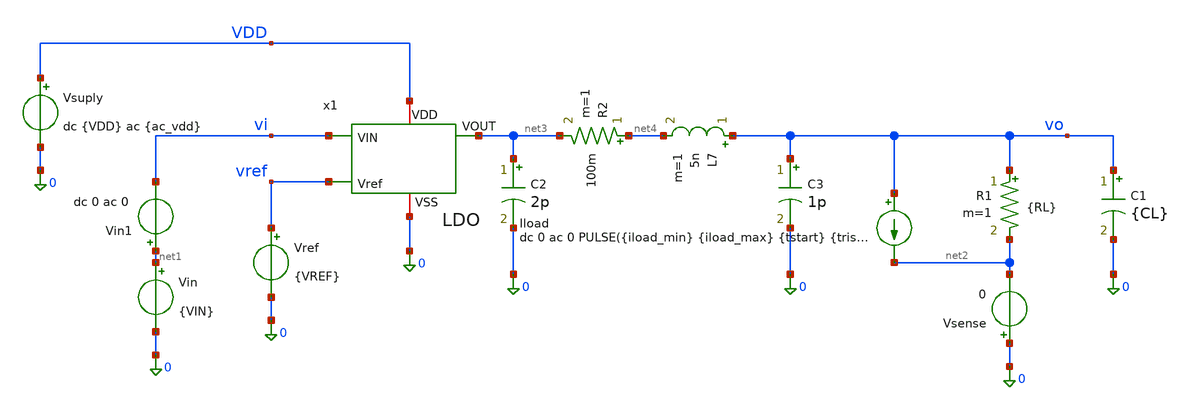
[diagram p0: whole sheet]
** sch_path: xschem/ldo_tb_montecarlo.sch
**.subckt ldo_tb_montecarlo
Vsuply VDD 0 dc {VDD} ac {ac_vdd}
Vref vref 0 {VREF}
Vin net1 0 {VIN}
Vin1 net1 vi dc 0 ac 0
x1 vi net3 VDD vref 0 LDO
R1 vo net2 {RL} m=1
C1 vo 0 {CL} m=1
Iload vo net2 dc 0 ac 0 PULSE({iload_min} {iload_max} {tstart} {trise} {tfall} {twidth} {tperiod})
Vsense 0 net2 0
C2 net3 0 2p m=1
R2 net4 net3 100m m=1
L7 vo net4 5n m=1
C3 vo 0 1p m=1
**** begin user architecture code






.lib /foss/pdks/sky130A/libs.tech/ngspice/sky130.lib.spice tt_mm
.option temp=27
.option num_threads=8
.param rsh_var = agauss(0, 0.005, 1)

* Forzar un punto de partida para ayudar a la convergencia
.nodeset V(VO)=1.2
.nodeset V(x1.Vre)=0.6


**parametros_ldo
.param VDD = 1.8
.param VREF = 0.6
.param VIN = '1*VDD'
.param RL = 240
.param CL = 1u
.param tsim = 2m

* Parámetros para la prueba de carga del LDO
.param iload_min = 1u
.param iload_max = 5m
.param tstart   = 30u
.param trise    = 100n
.param tfall    = 100n
.param twidth   = 100u
.param tperiod  = 200u

.param tsim = '3*tperiod'

.param ac_iprobe = 1
.param ac_vdd = 0

.control
* =========================================================
* CONFIGURACION DEL BUCLE MONTE CARLO
* =========================================================
let mc_runs = 300
let run = 1

set appendwrite
set filetype=ascii

let tperiod = 200u
let tsim = '3*tperiod'

echo === INICIO MONTE CARLO === > datos_mc.txt

* =========================================================
* INICIO DEL BUCLE
* =========================================================
while run <= mc_runs

    echo ======================================
    echo CORRIENDO MONTE CARLO ITERACION: $&run
    echo ======================================
    echo --- ITERACION: $&run --- >> datos_mc.txt

    * -----------------------------------------------------
    * 1. PREPARAR EL CHIP PARA ESTA ITERACION
    * -----------------------------------------------------
    * Limpiamos memoria y tiramos los dados estadísticos UNA VEZ
    reset

    * Bloqueamos la semilla estadística para que los siguientes 'reset'
    * evalúen exactamente las mismas variaciones físicas (el mismo chip).
    set mc_strict = 1

    * -----------------------------------------------------
    * B. TRANSIENTE (Overshoot y Undershoot)
    * -----------------------------------------------------
    alterparam ac_iprobe = 0
    alterparam ac_vdd = 0
    alterparam RL = 240e9
    reset

    tran 1u $&tsim

    * Acortamos los primeros 150us para evadir el pico del startup
    let t_ignorar = 150u

    meas tran v_estable_ligera FIND v(vo) AT=270u
    meas tran v_estable_pesada FIND v(vo) AT=180u
    meas tran vo_max MAX v(vo) from=$&t_ignorar to=$&tsim
    meas tran vo_min MIN v(vo) from=$&t_ignorar to=$&tsim
    meas tran salida_tran avg v(vo) from=$&t_ignorar to=$&tsim

    let undershoot_mV = (v_estable_ligera - vo_min) * 1e3
    let overshoot_mV = (vo_max - v_estable_pesada) * 1e3

    echo 'undershoot_mV = $&undershoot_mV' >> datos_mc.txt
    echo 'overshoot_mV = $&overshoot_mV' >> datos_mc.txt
    echo 'salida_tran = $&salida_tran' >> datos_mc.txt



    * -----------------------------------------------------
    * C. AC (Estabilidad)
    * -----------------------------------------------------
    alterparam ac_iprobe = 1
    alterparam ac_vdd = 0
    alterparam RL = 240
    reset
    alter @Iload[dc] = 10m

    ac dec 10 1 1G
    let T_loop = v(x1.vre) / v(x1.vre2)
    let ldb = vdb(T_loop)
    let fase = vp(T_loop) * 180 / pi

    meas ac ugb WHEN ldb = 0.0
    meas ac fase_ugb FIND fase WHEN ldb = 0.0
    let margen_fase = fase_ugb
    meas ac ganancia_banda_plana find ldb at=1

    echo 'margen_fase = $&margen_fase' >> datos_mc.txt
    echo 'ganancia_banda_plana = $&ganancia_banda_plana' >> datos_mc.txt
    echo 'ugb = $&ugb' >> datos_mc.txt

    * -----------------------------------------------------
    * E. AC (PSRR)
    * -----------------------------------------------------
    alterparam ac_iprobe = 0
    alterparam ac_vdd = 1
    alterparam RL = 240
    reset
    alter @Iload[dc] = 10m

    ac dec 10 10 1G
    let psrr1 = v(vdd)/v(vo)
    let psrr_db = vdb(psrr1)

    meas ac gananciaPSRR_1   find psrr_db at=10
    meas ac gananciaPSRR_1k  find psrr_db at=1k
    meas ac gananciaPSRR_10k find psrr_db at=10k
    meas ac gananciaPSRR_1M  find psrr_db at=1Meg

    echo 'psrr_1 = $&gananciaPSRR_1' >> datos_mc.txt
    echo 'psrr_1k = $&gananciaPSRR_1k' >> datos_mc.txt
    echo 'psrr_10k = $&gananciaPSRR_10k' >> datos_mc.txt
    echo 'psrr_1M = $&gananciaPSRR_1M' >> datos_mc.txt

    * -----------------------------------------------------
    * D. TRANSIENTE (Line Regulation)
    * -----------------------------------------------------
    alterparam ac_iprobe = 0
    alterparam ac_vdd = 0
    alterparam RL = 240
    reset

    alter @Vin[pwl] = [ 0 1.4 1m 1.8 ]
    alter @Iload[pwl] = [ 0 1u 1m 1u ]

    tran 1u 1m

    let t_line_ini = 40u
    let t_line_fin = 950u

    meas tran voline_max MAX v(vo) from=$&t_line_ini to=$&t_line_fin
    meas tran voline_min MIN v(vo) from=$&t_line_ini to=$&t_line_fin
    meas tran salida_line avg v(vo) from=$&t_line_ini to=$&t_line_fin
    let line_regulation_mV = (voline_max - voline_min)*1000

    echo 'line_regulation_mv = $&line_regulation_mV' >> datos_mc.txt
    echo 'salida_line = $&salida_line' >> datos_mc.txt

    * -----------------------------------------------------
    * F. TRANSIENTE (Load Regulation)
    * -----------------------------------------------------
    reset

    alter @Iload[pwl] = [ 0 1u 1m 5m ]
    alterparam RL = 240e3

    tran 1u 1m

    meas tran vout_light FIND v(vo) AT=40u
    meas tran vout_heavy FIND v(vo) AT=1m

    let load_regulation_mV = (vout_light - vout_heavy) * 1000

    echo 'load_regulation_mV = $&load_regulation_mV' >> datos_mc.txt

    * -----------------------------------------------------
    * G. TRANSIENTE (Dropout)
    * -----------------------------------------------------
    alterparam RL = 240
    reset

    alter @Vin[pwl] = [ 0 2 1m 0 ]
    alter @Iload[pwl] = [ 0 1u 1m 1u ]

    tran 1u 1m

    meas tran vout_nom FIND v(vo) AT=225u
    let vout_target = vout_nom * 0.95

    meas tran vin_do FIND v(vi) WHEN v(vo) = vout_target fall=1
    let dropout_mV = (vin_do - vout_target) * 1e3

    echo 'dropout_mV = $&dropout_mV' >> datos_mc.txt

    * -----------------------------------------------------
    * IMPORTANTE: Desbloquear la semilla para la siguiente iteración
    * -----------------------------------------------------
    unset mc_strict

    let run = run + 1
end

echo === FIN MONTE CARLO === >> datos_mc.txt
echo ======================================
echo SIMULACION MONTE CARLO FINALIZADA
echo ======================================
.endc









**** end user architecture code
**.ends

* expanding   symbol:  /foss/designs/LDO-sky130/xschem/LDO.sym # of pins=5
** sym_path: xschem/LDO.sym
** sch_path: xschem/LDO.sch
.subckt LDO VIN VOUT VDD Vref VSS
*.ipin VIN
*.iopin VDD
*.opin VOUT
*.ipin Vref
*.iopin VSS
V1 vre2 Vre 0 ac {ac_iprobe}
x1 VDD Vgp Vref vre2 VSS Vgn_bias OTA
XC1 VOUT Vre sky130_fd_pr__cap_mim_m3_2 W=27 L=25 MF=1 m=1
XM1 VOUT Vgp VIN VDD sky130_fd_pr__pfet_01v8_lvt L=0.5 W=250 nf=100 ad='int((100 + 1)/2) * 250 / 100 * 0.29'
+ as='int((100 + 2)/2) * 250 / 100 * 0.29' pd='2*int((100 + 1)/2) * (250 / 100 + 0.29)' ps='2*int((100 + 2)/2) * (250 / 100 + 0.29)'
+ nrd='0.29 / 250 ' nrs='0.29 / 250 ' sa=0 sb=0 sd=0 mult=5 m=5
x2 VDD Vgn_bias VSS self_bias
R8 VOUT Vre {109k*(1+rsh_var)} m=1
R9 Vre VSS {109k*(1+rsh_var)} m=1
.ends


* expanding   symbol:  /foss/designs/LDO-sky130/xschem/OTA.sym # of pins=6
** sym_path: xschem/OTA/OTA.sym
** sch_path: xschem/OTA/OTA.sch
.subckt OTA VDD VO_ota VIN_ota VIP_ota VSS VGN
*.ipin VIN_ota
*.opin VO_ota
*.iopin VSS
*.iopin VDD
*.ipin VIP_ota
*.iopin VGN
XMpr vo1 vd VSS VSS sky130_fd_pr__nfet_01v8 L=1 W=6 nf=4 ad='int((4 + 1)/2) * 6 / 4 * 0.29' as='int((4 + 2)/2) * 6 / 4 * 0.29'
+ pd='2*int((4 + 1)/2) * (6 / 4 + 0.29)' ps='2*int((4 + 2)/2) * (6 / 4 + 0.29)' nrd='0.29 / 6 ' nrs='0.29 / 6 '
+ sa=0 sb=0 sd=0 mult=1 m=1
XMnr vd vd VSS VSS sky130_fd_pr__nfet_01v8 L=1 W=6 nf=4 ad='int((4 + 1)/2) * 6 / 4 * 0.29' as='int((4 + 2)/2) * 6 / 4 * 0.29'
+ pd='2*int((4 + 1)/2) * (6 / 4 + 0.29)' ps='2*int((4 + 2)/2) * (6 / 4 + 0.29)' nrd='0.29 / 6 ' nrs='0.29 / 6 '
+ sa=0 sb=0 sd=0 mult=1 m=1
XMo VO_ota vo1 VSS VSS sky130_fd_pr__nfet_01v8 L=2 W=8 nf=8 ad='int((8 + 1)/2) * 8 / 8 * 0.29' as='int((8 + 2)/2) * 8 / 8 * 0.29'
+ pd='2*int((8 + 1)/2) * (8 / 8 + 0.29)' ps='2*int((8 + 2)/2) * (8 / 8 + 0.29)' nrd='0.29 / 8 ' nrs='0.29 / 8 '
+ sa=0 sb=0 sd=0 mult=1 m=1
XMrc2 VO_ota vgp VDD VDD sky130_fd_pr__pfet_01v8_lvt L=2 W=50 nf=8 ad='int((8 + 1)/2) * 50 / 8 * 0.29'
+ as='int((8 + 2)/2) * 50 / 8 * 0.29' pd='2*int((8 + 1)/2) * (50 / 8 + 0.29)' ps='2*int((8 + 2)/2) * (50 / 8 + 0.29)'
+ nrd='0.29 / 50 ' nrs='0.29 / 50 ' sa=0 sb=0 sd=0 mult=1 m=1
XC1 VO_ota vmiler sky130_fd_pr__cap_mim_m3_2 W=44.6 L=56 MF=1 m=1
XMp vo1 VIP_ota vtail VDD sky130_fd_pr__pfet_01v8_lvt L=1 W=26 nf=4 ad='int((4 + 1)/2) * 26 / 4 * 0.29'
+ as='int((4 + 2)/2) * 26 / 4 * 0.29' pd='2*int((4 + 1)/2) * (26 / 4 + 0.29)' ps='2*int((4 + 2)/2) * (26 / 4 + 0.29)'
+ nrd='0.29 / 26 ' nrs='0.29 / 26 ' sa=0 sb=0 sd=0 mult=1 m=1
XMn vd VIN_ota vtail VDD sky130_fd_pr__pfet_01v8_lvt L=1 W=26 nf=4 ad='int((4 + 1)/2) * 26 / 4 * 0.29'
+ as='int((4 + 2)/2) * 26 / 4 * 0.29' pd='2*int((4 + 1)/2) * (26 / 4 + 0.29)' ps='2*int((4 + 2)/2) * (26 / 4 + 0.29)'
+ nrd='0.29 / 26 ' nrs='0.29 / 26 ' sa=0 sb=0 sd=0 mult=1 m=1
XMrc1 vtail vgp VDD VDD sky130_fd_pr__pfet_01v8_lvt L=1 W=50 nf=8 ad='int((8 + 1)/2) * 50 / 8 * 0.29'
+ as='int((8 + 2)/2) * 50 / 8 * 0.29' pd='2*int((8 + 1)/2) * (50 / 8 + 0.29)' ps='2*int((8 + 2)/2) * (50 / 8 + 0.29)'
+ nrd='0.29 / 50 ' nrs='0.29 / 50 ' sa=0 sb=0 sd=0 mult=1 m=1
XMr vgp vgp VDD VDD sky130_fd_pr__pfet_01v8_lvt L=1 W=12.5 nf=2 ad='int((2 + 1)/2) * 12.5 / 2 * 0.29'
+ as='int((2 + 2)/2) * 12.5 / 2 * 0.29' pd='2*int((2 + 1)/2) * (12.5 / 2 + 0.29)' ps='2*int((2 + 2)/2) * (12.5 / 2 + 0.29)'
+ nrd='0.29 / 12.5 ' nrs='0.29 / 12.5 ' sa=0 sb=0 sd=0 mult=1 m=1
XMnref vgp VGN VSS VSS sky130_fd_pr__nfet_01v8 L=1 W=8 nf=1 ad='int((1 + 1)/2) * 8 / 1 * 0.29' as='int((1 + 2)/2) * 8 / 1 * 0.29'
+ pd='2*int((1 + 1)/2) * (8 / 1 + 0.29)' ps='2*int((1 + 2)/2) * (8 / 1 + 0.29)' nrd='0.29 / 8 ' nrs='0.29 / 8 '
+ sa=0 sb=0 sd=0 mult=1 m=1
XR10 vo1 vmiler VSS sky130_fd_pr__res_xhigh_po_0p35 L=90.72 mult=1 m=1
.ends


* expanding   symbol:  /foss/designs/OSCAR/xschem/Iref/self_bias.sym # of pins=3
** sym_path: xschem/Iref/self_bias.sym
** sch_path: xschem/Iref/self_bias.sch
.subckt self_bias VDD VR VSS
*.iopin VR
*.iopin VDD
*.iopin VSS
XMp4 vgp_self vgp_self VDD VDD sky130_fd_pr__pfet_01v8_lvt L=1 W=30 nf=6 ad='int((6 + 1)/2) * 30 / 6 * 0.29'
+ as='int((6 + 2)/2) * 30 / 6 * 0.29' pd='2*int((6 + 1)/2) * (30 / 6 + 0.29)' ps='2*int((6 + 2)/2) * (30 / 6 + 0.29)'
+ nrd='0.29 / 30 ' nrs='0.29 / 30 ' sa=0 sb=0 sd=0 mult=1 m=1
XMp3 VDI vgp_self VDD VDD sky130_fd_pr__pfet_01v8_lvt L=1 W=30 nf=6 ad='int((6 + 1)/2) * 30 / 6 * 0.29'
+ as='int((6 + 2)/2) * 30 / 6 * 0.29' pd='2*int((6 + 1)/2) * (30 / 6 + 0.29)' ps='2*int((6 + 2)/2) * (30 / 6 + 0.29)'
+ nrd='0.29 / 30 ' nrs='0.29 / 30 ' sa=0 sb=0 sd=0 mult=1 m=1
XMs2 VDinv VR vp1 VDD sky130_fd_pr__pfet_01v8_lvt L=5 W=0.5 nf=1 ad='int((1 + 1)/2) * 0.5 / 1 * 0.29'
+ as='int((1 + 2)/2) * 0.5 / 1 * 0.29' pd='2*int((1 + 1)/2) * (0.5 / 1 + 0.29)' ps='2*int((1 + 2)/2) * (0.5 / 1 + 0.29)'
+ nrd='0.29 / 0.5 ' nrs='0.29 / 0.5 ' sa=0 sb=0 sd=0 mult=1 m=1
XMn2 vgp_self VDI VR VSS sky130_fd_pr__nfet_01v8 L=1 W=24 nf=6 ad='int((6 + 1)/2) * 24 / 6 * 0.29' as='int((6 + 2)/2) * 24 / 6 * 0.29'
+ pd='2*int((6 + 1)/2) * (24 / 6 + 0.29)' ps='2*int((6 + 2)/2) * (24 / 6 + 0.29)' nrd='0.29 / 24 ' nrs='0.29 / 24 '
+ sa=0 sb=0 sd=0 mult=1 m=1
XMn1 VDI VR VSS VSS sky130_fd_pr__nfet_01v8 L=1 W=5 nf=5 ad='int((5 + 1)/2) * 5 / 5 * 0.29' as='int((5 + 2)/2) * 5 / 5 * 0.29'
+ pd='2*int((5 + 1)/2) * (5 / 5 + 0.29)' ps='2*int((5 + 2)/2) * (5 / 5 + 0.29)' nrd='0.29 / 5 ' nrs='0.29 / 5 '
+ sa=0 sb=0 sd=0 mult=1 m=1
XMs3 VDinv VR VSS VSS sky130_fd_pr__nfet_01v8 L=1 W=20 nf=5 ad='int((5 + 1)/2) * 20 / 5 * 0.29' as='int((5 + 2)/2) * 20 / 5 * 0.29'
+ pd='2*int((5 + 1)/2) * (20 / 5 + 0.29)' ps='2*int((5 + 2)/2) * (20 / 5 + 0.29)' nrd='0.29 / 20 ' nrs='0.29 / 20 '
+ sa=0 sb=0 sd=0 mult=1 m=1
XMs1 vgp_self VDinv VSS VSS sky130_fd_pr__nfet_01v8 L=1 W=2 nf=2 ad='int((2 + 1)/2) * 2 / 2 * 0.29' as='int((2 + 2)/2) * 2 / 2 * 0.29'
+ pd='2*int((2 + 1)/2) * (2 / 2 + 0.29)' ps='2*int((2 + 2)/2) * (2 / 2 + 0.29)' nrd='0.29 / 2 ' nrs='0.29 / 2 '
+ sa=0 sb=0 sd=0 mult=1 m=1
XR11 VSS VR VSS sky130_fd_pr__res_xhigh_po_0p69 L=20.7 mult=1 m=1
XMs4 vp1 VR vp2 VDD sky130_fd_pr__pfet_01v8_lvt L=5 W=0.5 nf=1 ad='int((1 + 1)/2) * 0.5 / 1 * 0.29' as='int((1 + 2)/2) * 0.5 / 1 * 0.29'
+ pd='2*int((1 + 1)/2) * (0.5 / 1 + 0.29)' ps='2*int((1 + 2)/2) * (0.5 / 1 + 0.29)' nrd='0.29 / 0.5 ' nrs='0.29 / 0.5 '
+ sa=0 sb=0 sd=0 mult=1 m=1
XMs5 vp2 VR vp3 VDD sky130_fd_pr__pfet_01v8_lvt L=5 W=0.5 nf=1 ad='int((1 + 1)/2) * 0.5 / 1 * 0.29' as='int((1 + 2)/2) * 0.5 / 1 * 0.29'
+ pd='2*int((1 + 1)/2) * (0.5 / 1 + 0.29)' ps='2*int((1 + 2)/2) * (0.5 / 1 + 0.29)' nrd='0.29 / 0.5 ' nrs='0.29 / 0.5 '
+ sa=0 sb=0 sd=0 mult=1 m=1
XMs6 vp3 VR vp4 VDD sky130_fd_pr__pfet_01v8_lvt L=5 W=0.5 nf=1 ad='int((1 + 1)/2) * 0.5 / 1 * 0.29' as='int((1 + 2)/2) * 0.5 / 1 * 0.29'
+ pd='2*int((1 + 1)/2) * (0.5 / 1 + 0.29)' ps='2*int((1 + 2)/2) * (0.5 / 1 + 0.29)' nrd='0.29 / 0.5 ' nrs='0.29 / 0.5 '
+ sa=0 sb=0 sd=0 mult=1 m=1
XMs7 vp4 VR VDD VDD sky130_fd_pr__pfet_01v8_lvt L=5 W=0.5 nf=1 ad='int((1 + 1)/2) * 0.5 / 1 * 0.29' as='int((1 + 2)/2) * 0.5 / 1 * 0.29'
+ pd='2*int((1 + 1)/2) * (0.5 / 1 + 0.29)' ps='2*int((1 + 2)/2) * (0.5 / 1 + 0.29)' nrd='0.29 / 0.5 ' nrs='0.29 / 0.5 '
+ sa=0 sb=0 sd=0 mult=1 m=1
.ends

.end
